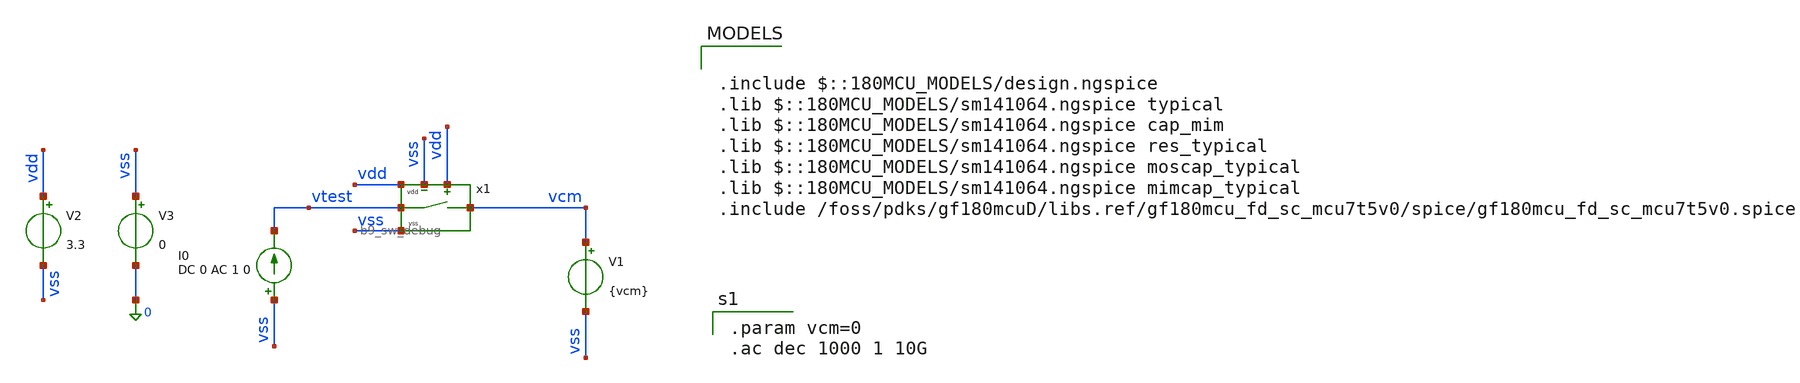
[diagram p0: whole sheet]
** sch_path: xschem/sw/b9_sw_debug_tb_basic.sch
**.subckt b9_sw_debug_tb_basic
V1 vcm vss {vcm}
I0 vss vtest DC 0 AC 1 0
V2 vdd vss 3.3
V3 vss 0 0
x1 vdd vtest vss vcm vss vdd b9_sw_debug
**** begin user architecture code

.include $::180MCU_MODELS/design.ngspice
.lib $::180MCU_MODELS/sm141064.ngspice typical
.lib $::180MCU_MODELS/sm141064.ngspice cap_mim
.lib $::180MCU_MODELS/sm141064.ngspice res_typical
.lib $::180MCU_MODELS/sm141064.ngspice moscap_typical
.lib $::180MCU_MODELS/sm141064.ngspice mimcap_typical
.include /foss/pdks/gf180mcuD/libs.ref/gf180mcu_fd_sc_mcu7t5v0/spice/gf180mcu_fd_sc_mcu7t5v0.spice


.param vcm=0
.ac dec 1000 1 10G

**** end user architecture code
**.ends

* expanding   symbol:  xschem/sw/b9_sw_debug.sym # of pins=6
** sym_path: xschem/sw/b9_sw_debug.sym
** sch_path: xschem/sw/b9_sw_debug.sch
.subckt b9_sw_debug vdd va vss vb en_n en
*.iopin vdd
*.iopin vss
*.iopin en
*.iopin va
*.iopin vb
*.iopin en_n
XM1 vb en va vss nfet_03v3 L=0.28u W=3.2u nf=4 ad='int((nf+1)/2) * W/nf * 0.18u' as='int((nf+2)/2) * W/nf * 0.18u'
+ pd='2*int((nf+1)/2) * (W/nf + 0.18u)' ps='2*int((nf+2)/2) * (W/nf + 0.18u)' nrd='0.18u / W' nrs='0.18u / W'
+ sa=0 sb=0 sd=0 m=1
XM2 va en_n vb vdd pfet_03v3 L=0.28u W=9.6u nf=4 ad='int((nf+1)/2) * W/nf * 0.18u' as='int((nf+2)/2) * W/nf * 0.18u'
+ pd='2*int((nf+1)/2) * (W/nf + 0.18u)' ps='2*int((nf+2)/2) * (W/nf + 0.18u)' nrd='0.18u / W' nrs='0.18u / W'
+ sa=0 sb=0 sd=0 m=1
.ends

.end
